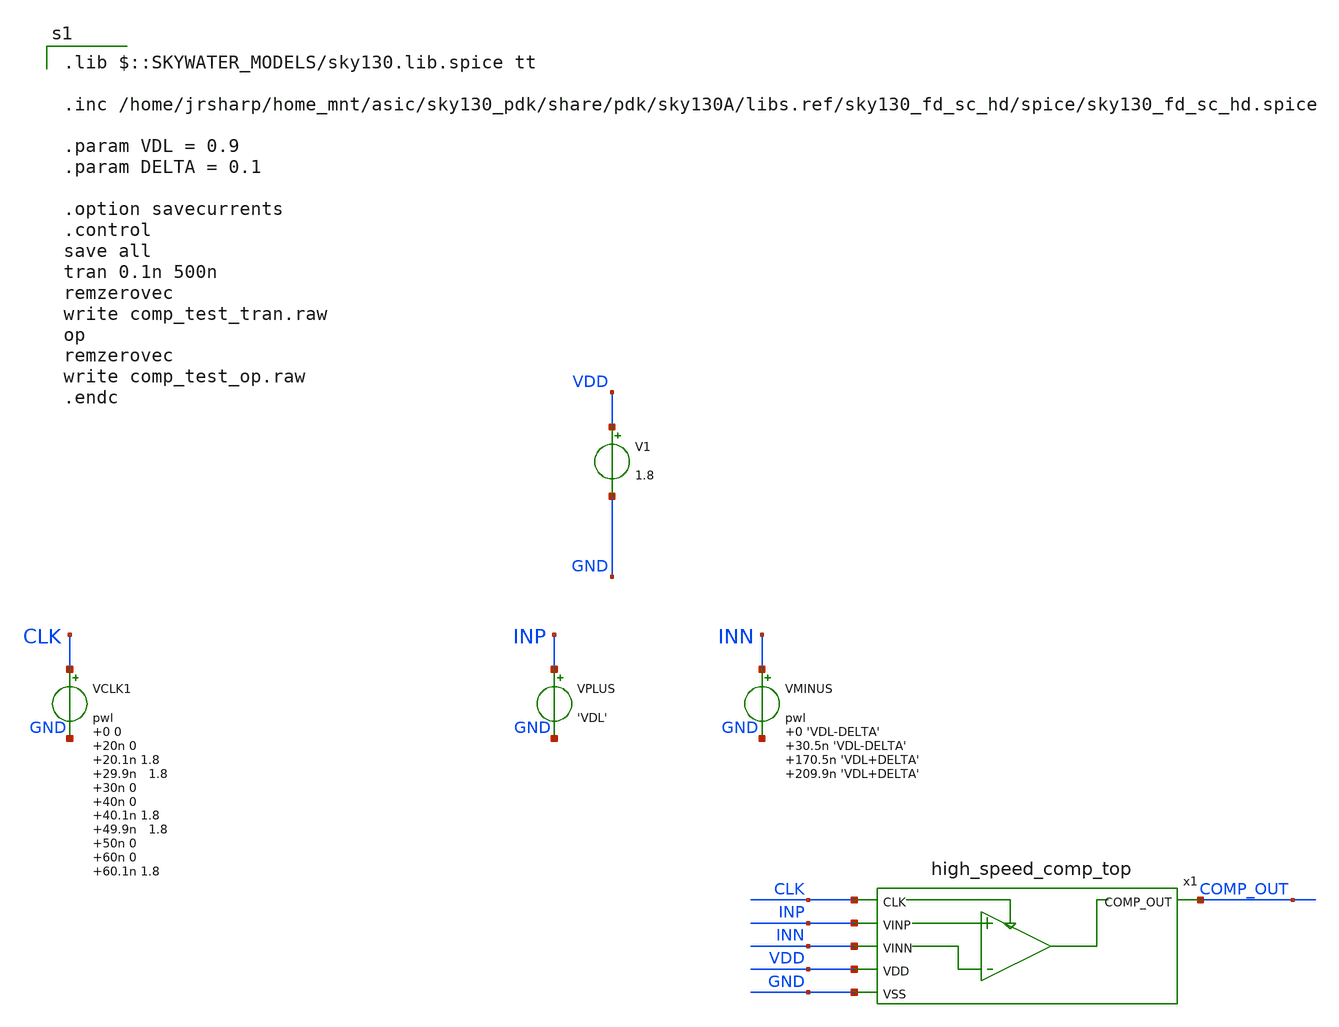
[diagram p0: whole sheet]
** sch_path: xschem/high_speed_comp_test.sch
**.subckt high_speed_comp_test
V1 VDD GND 1.8
VPLUS INP GND 'VDL'
VMINUS INN GND pwl 0 'VDL-DELTA' 30.5n 'VDL-DELTA' 170.5n 'VDL+DELTA' 209.9n 'VDL+DELTA'

VCLK1 CLK GND pwl 0 0 20n 0 20.1n 1.8 29.9n 1.8 30n 0 40n 0 40.1n 1.8 49.9n 1.8 50n 0 60n 0 60.1n
+ 1.8 69.9n 1.8 70n 0 80n 0 80.1n 1.8 89.9n 1.8 90n 0 100n 0 100.1n 1.8 109.9n 1.8 110n 0 120n 0 120.1n
+ 1.8 129.9n 1.8 130n 0 140n 0 140.1n 1.8 149.9n 1.8 150n 0 160n 0 160.1n 1.8 169.9n 1.8 170n 0 180n 0
+ 180.1n 1.8 189.9n 1.8 190n 0 200n 0 200.1n 1.8 209.9n 1.8 210n 0 220n 0 220.1n 1.8 229.9n 1.8 230n 0 240n
+ 0

x1 CLK INP INN VDD COMP_OUT GND high_speed_comp_top
**** begin user architecture code
 .lib $::SKYWATER_MODELS/sky130.lib.spice tt

.inc /home/jrsharp/home_mnt/asic/sky130_pdk/share/pdk/sky130A/libs.ref/sky130_fd_sc_hd/spice/sky130_fd_sc_hd.spice

.param VDL = 0.9
.param DELTA = 0.1

.option savecurrents
.control
save all
tran 0.1n 500n
remzerovec
write comp_test_tran.raw
op
remzerovec
write comp_test_op.raw
.endc



**** end user architecture code
**.ends
.end
